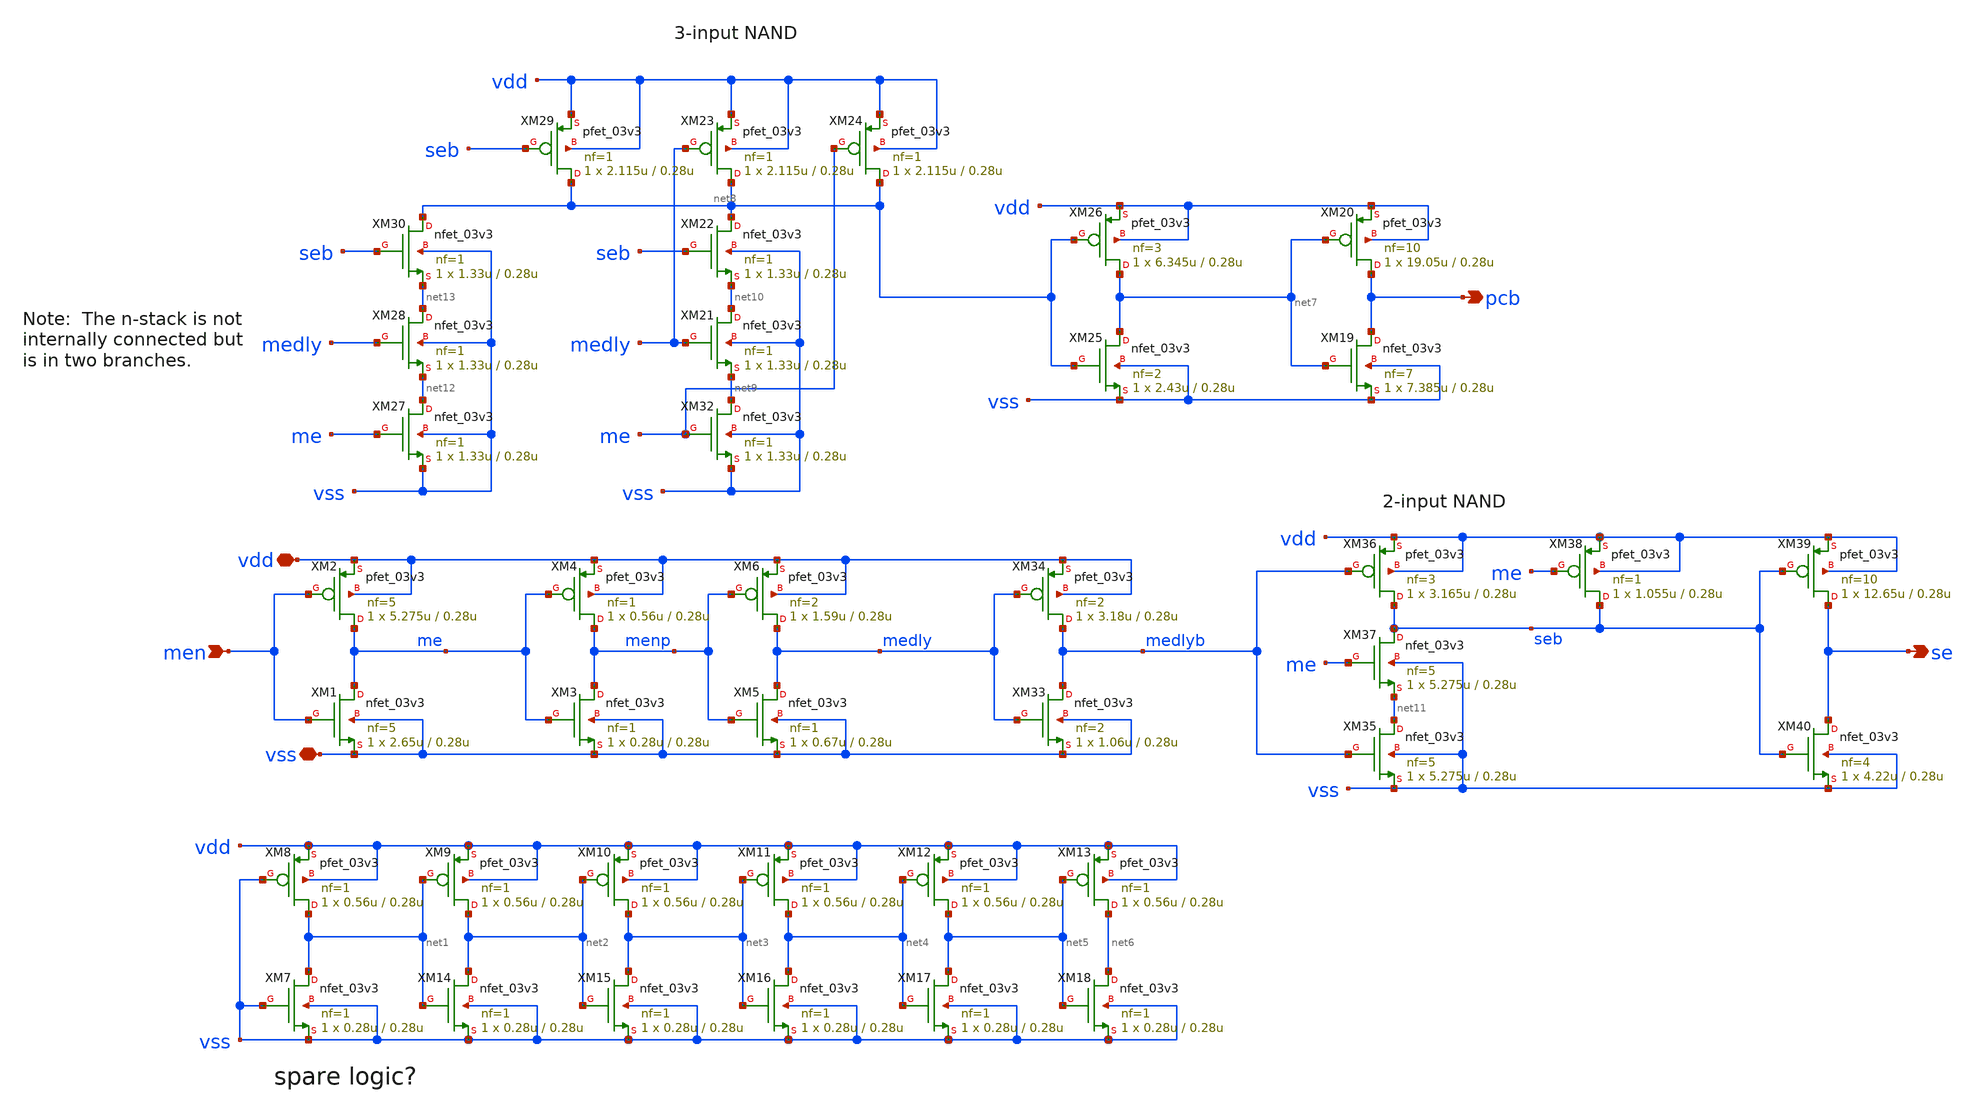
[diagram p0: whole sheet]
** sch_path: cells/gf180mcu_ocd_ip_sram__sram512x8m8wm1/xschem/sacntl_2_3v512x8m81.sch
**.subckt sacntl_2_3v512x8m81 men vdd vss se pcb
*.ipin men
*.iopin vdd
*.iopin vss
*.opin se
*.opin pcb
XM1 me men vss vss nfet_03v3 L=0.28u W=2.65u nf=5 ad='int((nf+1)/2) * W/nf * 0.18u' as='int((nf+2)/2) * W/nf * 0.18u'
+ pd='2*int((nf+1)/2) * (W/nf + 0.18u)' ps='2*int((nf+2)/2) * (W/nf + 0.18u)' nrd='0.18u / W' nrs='0.18u / W'
+ sa=0 sb=0 sd=0 m=1
XM2 me men vdd vdd pfet_03v3 L=0.28u W=5.275u nf=5 ad='int((nf+1)/2) * W/nf * 0.18u' as='int((nf+2)/2) * W/nf * 0.18u'
+ pd='2*int((nf+1)/2) * (W/nf + 0.18u)' ps='2*int((nf+2)/2) * (W/nf + 0.18u)' nrd='0.18u / W' nrs='0.18u / W'
+ sa=0 sb=0 sd=0 m=1
XM3 menp me vss vss nfet_03v3 L=0.28u W=0.28u nf=1 ad='int((nf+1)/2) * W/nf * 0.18u' as='int((nf+2)/2) * W/nf * 0.18u'
+ pd='2*int((nf+1)/2) * (W/nf + 0.18u)' ps='2*int((nf+2)/2) * (W/nf + 0.18u)' nrd='0.18u / W' nrs='0.18u / W'
+ sa=0 sb=0 sd=0 m=1
XM4 menp me vdd vdd pfet_03v3 L=0.28u W=0.56u nf=1 ad='int((nf+1)/2) * W/nf * 0.18u' as='int((nf+2)/2) * W/nf * 0.18u'
+ pd='2*int((nf+1)/2) * (W/nf + 0.18u)' ps='2*int((nf+2)/2) * (W/nf + 0.18u)' nrd='0.18u / W' nrs='0.18u / W'
+ sa=0 sb=0 sd=0 m=1
XM5 medly menp vss vss nfet_03v3 L=0.28u W=0.67u nf=1 ad='int((nf+1)/2) * W/nf * 0.18u' as='int((nf+2)/2) * W/nf * 0.18u'
+ pd='2*int((nf+1)/2) * (W/nf + 0.18u)' ps='2*int((nf+2)/2) * (W/nf + 0.18u)' nrd='0.18u / W' nrs='0.18u / W'
+ sa=0 sb=0 sd=0 m=1
XM6 medly menp vdd vdd pfet_03v3 L=0.28u W=1.59u nf=2 ad='int((nf+1)/2) * W/nf * 0.18u' as='int((nf+2)/2) * W/nf * 0.18u'
+ pd='2*int((nf+1)/2) * (W/nf + 0.18u)' ps='2*int((nf+2)/2) * (W/nf + 0.18u)' nrd='0.18u / W' nrs='0.18u / W'
+ sa=0 sb=0 sd=0 m=1
XM7 net1 vss vss vss nfet_03v3 L=0.28u W=0.28u nf=1 ad='int((nf+1)/2) * W/nf * 0.18u' as='int((nf+2)/2) * W/nf * 0.18u'
+ pd='2*int((nf+1)/2) * (W/nf + 0.18u)' ps='2*int((nf+2)/2) * (W/nf + 0.18u)' nrd='0.18u / W' nrs='0.18u / W'
+ sa=0 sb=0 sd=0 m=1
XM8 net1 vss vdd vdd pfet_03v3 L=0.28u W=0.56u nf=1 ad='int((nf+1)/2) * W/nf * 0.18u' as='int((nf+2)/2) * W/nf * 0.18u'
+ pd='2*int((nf+1)/2) * (W/nf + 0.18u)' ps='2*int((nf+2)/2) * (W/nf + 0.18u)' nrd='0.18u / W' nrs='0.18u / W'
+ sa=0 sb=0 sd=0 m=1
XM9 net2 net1 vdd vdd pfet_03v3 L=0.28u W=0.56u nf=1 ad='int((nf+1)/2) * W/nf * 0.18u' as='int((nf+2)/2) * W/nf * 0.18u'
+ pd='2*int((nf+1)/2) * (W/nf + 0.18u)' ps='2*int((nf+2)/2) * (W/nf + 0.18u)' nrd='0.18u / W' nrs='0.18u / W'
+ sa=0 sb=0 sd=0 m=1
XM10 net3 net2 vdd vdd pfet_03v3 L=0.28u W=0.56u nf=1 ad='int((nf+1)/2) * W/nf * 0.18u' as='int((nf+2)/2) * W/nf * 0.18u'
+ pd='2*int((nf+1)/2) * (W/nf + 0.18u)' ps='2*int((nf+2)/2) * (W/nf + 0.18u)' nrd='0.18u / W' nrs='0.18u / W'
+ sa=0 sb=0 sd=0 m=1
XM11 net4 net3 vdd vdd pfet_03v3 L=0.28u W=0.56u nf=1 ad='int((nf+1)/2) * W/nf * 0.18u' as='int((nf+2)/2) * W/nf * 0.18u'
+ pd='2*int((nf+1)/2) * (W/nf + 0.18u)' ps='2*int((nf+2)/2) * (W/nf + 0.18u)' nrd='0.18u / W' nrs='0.18u / W'
+ sa=0 sb=0 sd=0 m=1
XM12 net5 net4 vdd vdd pfet_03v3 L=0.28u W=0.56u nf=1 ad='int((nf+1)/2) * W/nf * 0.18u' as='int((nf+2)/2) * W/nf * 0.18u'
+ pd='2*int((nf+1)/2) * (W/nf + 0.18u)' ps='2*int((nf+2)/2) * (W/nf + 0.18u)' nrd='0.18u / W' nrs='0.18u / W'
+ sa=0 sb=0 sd=0 m=1
XM13 net6 net5 vdd vdd pfet_03v3 L=0.28u W=0.56u nf=1 ad='int((nf+1)/2) * W/nf * 0.18u' as='int((nf+2)/2) * W/nf * 0.18u'
+ pd='2*int((nf+1)/2) * (W/nf + 0.18u)' ps='2*int((nf+2)/2) * (W/nf + 0.18u)' nrd='0.18u / W' nrs='0.18u / W'
+ sa=0 sb=0 sd=0 m=1
XM14 net2 net1 vss vss nfet_03v3 L=0.28u W=0.28u nf=1 ad='int((nf+1)/2) * W/nf * 0.18u' as='int((nf+2)/2) * W/nf * 0.18u'
+ pd='2*int((nf+1)/2) * (W/nf + 0.18u)' ps='2*int((nf+2)/2) * (W/nf + 0.18u)' nrd='0.18u / W' nrs='0.18u / W'
+ sa=0 sb=0 sd=0 m=1
XM15 net3 net2 vss vss nfet_03v3 L=0.28u W=0.28u nf=1 ad='int((nf+1)/2) * W/nf * 0.18u' as='int((nf+2)/2) * W/nf * 0.18u'
+ pd='2*int((nf+1)/2) * (W/nf + 0.18u)' ps='2*int((nf+2)/2) * (W/nf + 0.18u)' nrd='0.18u / W' nrs='0.18u / W'
+ sa=0 sb=0 sd=0 m=1
XM16 net4 net3 vss vss nfet_03v3 L=0.28u W=0.28u nf=1 ad='int((nf+1)/2) * W/nf * 0.18u' as='int((nf+2)/2) * W/nf * 0.18u'
+ pd='2*int((nf+1)/2) * (W/nf + 0.18u)' ps='2*int((nf+2)/2) * (W/nf + 0.18u)' nrd='0.18u / W' nrs='0.18u / W'
+ sa=0 sb=0 sd=0 m=1
XM17 net5 net4 vss vss nfet_03v3 L=0.28u W=0.28u nf=1 ad='int((nf+1)/2) * W/nf * 0.18u' as='int((nf+2)/2) * W/nf * 0.18u'
+ pd='2*int((nf+1)/2) * (W/nf + 0.18u)' ps='2*int((nf+2)/2) * (W/nf + 0.18u)' nrd='0.18u / W' nrs='0.18u / W'
+ sa=0 sb=0 sd=0 m=1
XM18 net6 net5 vss vss nfet_03v3 L=0.28u W=0.28u nf=1 ad='int((nf+1)/2) * W/nf * 0.18u' as='int((nf+2)/2) * W/nf * 0.18u'
+ pd='2*int((nf+1)/2) * (W/nf + 0.18u)' ps='2*int((nf+2)/2) * (W/nf + 0.18u)' nrd='0.18u / W' nrs='0.18u / W'
+ sa=0 sb=0 sd=0 m=1
XM19 pcb net7 vss vss nfet_03v3 L=0.28u W=7.385u nf=7 ad='int((nf+1)/2) * W/nf * 0.18u' as='int((nf+2)/2) * W/nf * 0.18u'
+ pd='2*int((nf+1)/2) * (W/nf + 0.18u)' ps='2*int((nf+2)/2) * (W/nf + 0.18u)' nrd='0.18u / W' nrs='0.18u / W'
+ sa=0 sb=0 sd=0 m=1
XM20 pcb net7 vdd vdd pfet_03v3 L=0.28u W=19.05u nf=10 ad='int((nf+1)/2) * W/nf * 0.18u' as='int((nf+2)/2) * W/nf * 0.18u'
+ pd='2*int((nf+1)/2) * (W/nf + 0.18u)' ps='2*int((nf+2)/2) * (W/nf + 0.18u)' nrd='0.18u / W' nrs='0.18u / W'
+ sa=0 sb=0 sd=0 m=1
XM25 net7 net8 vss vss nfet_03v3 L=0.28u W=2.43u nf=2 ad='int((nf+1)/2) * W/nf * 0.18u' as='int((nf+2)/2) * W/nf * 0.18u'
+ pd='2*int((nf+1)/2) * (W/nf + 0.18u)' ps='2*int((nf+2)/2) * (W/nf + 0.18u)' nrd='0.18u / W' nrs='0.18u / W'
+ sa=0 sb=0 sd=0 m=1
XM26 net7 net8 vdd vdd pfet_03v3 L=0.28u W=6.345u nf=3 ad='int((nf+1)/2) * W/nf * 0.18u' as='int((nf+2)/2) * W/nf * 0.18u'
+ pd='2*int((nf+1)/2) * (W/nf + 0.18u)' ps='2*int((nf+2)/2) * (W/nf + 0.18u)' nrd='0.18u / W' nrs='0.18u / W'
+ sa=0 sb=0 sd=0 m=1
XM29 net8 seb vdd vdd pfet_03v3 L=0.28u W=2.115u nf=1 ad='int((nf+1)/2) * W/nf * 0.18u' as='int((nf+2)/2) * W/nf * 0.18u'
+ pd='2*int((nf+1)/2) * (W/nf + 0.18u)' ps='2*int((nf+2)/2) * (W/nf + 0.18u)' nrd='0.18u / W' nrs='0.18u / W'
+ sa=0 sb=0 sd=0 m=1
XM32 net9 me vss vss nfet_03v3 L=0.28u W=1.33u nf=1 ad='int((nf+1)/2) * W/nf * 0.18u' as='int((nf+2)/2) * W/nf * 0.18u'
+ pd='2*int((nf+1)/2) * (W/nf + 0.18u)' ps='2*int((nf+2)/2) * (W/nf + 0.18u)' nrd='0.18u / W' nrs='0.18u / W'
+ sa=0 sb=0 sd=0 m=1
XM33 medlyb medly vss vss nfet_03v3 L=0.28u W=1.06u nf=2 ad='int((nf+1)/2) * W/nf * 0.18u' as='int((nf+2)/2) * W/nf * 0.18u'
+ pd='2*int((nf+1)/2) * (W/nf + 0.18u)' ps='2*int((nf+2)/2) * (W/nf + 0.18u)' nrd='0.18u / W' nrs='0.18u / W'
+ sa=0 sb=0 sd=0 m=1
XM34 medlyb medly vdd vdd pfet_03v3 L=0.28u W=3.18u nf=2 ad='int((nf+1)/2) * W/nf * 0.18u' as='int((nf+2)/2) * W/nf * 0.18u'
+ pd='2*int((nf+1)/2) * (W/nf + 0.18u)' ps='2*int((nf+2)/2) * (W/nf + 0.18u)' nrd='0.18u / W' nrs='0.18u / W'
+ sa=0 sb=0 sd=0 m=1
XM35 net11 medlyb vss vss nfet_03v3 L=0.28u W=5.275u nf=5 ad='int((nf+1)/2) * W/nf * 0.18u' as='int((nf+2)/2) * W/nf * 0.18u'
+ pd='2*int((nf+1)/2) * (W/nf + 0.18u)' ps='2*int((nf+2)/2) * (W/nf + 0.18u)' nrd='0.18u / W' nrs='0.18u / W'
+ sa=0 sb=0 sd=0 m=1
XM36 seb medlyb vdd vdd pfet_03v3 L=0.28u W=3.165u nf=3 ad='int((nf+1)/2) * W/nf * 0.18u' as='int((nf+2)/2) * W/nf * 0.18u'
+ pd='2*int((nf+1)/2) * (W/nf + 0.18u)' ps='2*int((nf+2)/2) * (W/nf + 0.18u)' nrd='0.18u / W' nrs='0.18u / W'
+ sa=0 sb=0 sd=0 m=1
XM37 seb me net11 vss nfet_03v3 L=0.28u W=5.275u nf=5 ad='int((nf+1)/2) * W/nf * 0.18u' as='int((nf+2)/2) * W/nf * 0.18u'
+ pd='2*int((nf+1)/2) * (W/nf + 0.18u)' ps='2*int((nf+2)/2) * (W/nf + 0.18u)' nrd='0.18u / W' nrs='0.18u / W'
+ sa=0 sb=0 sd=0 m=1
XM38 seb me vdd vdd pfet_03v3 L=0.28u W=1.055u nf=1 ad='int((nf+1)/2) * W/nf * 0.18u' as='int((nf+2)/2) * W/nf * 0.18u'
+ pd='2*int((nf+1)/2) * (W/nf + 0.18u)' ps='2*int((nf+2)/2) * (W/nf + 0.18u)' nrd='0.18u / W' nrs='0.18u / W'
+ sa=0 sb=0 sd=0 m=1
XM39 se seb vdd vdd pfet_03v3 L=0.28u W=12.65u nf=10 ad='int((nf+1)/2) * W/nf * 0.18u' as='int((nf+2)/2) * W/nf * 0.18u'
+ pd='2*int((nf+1)/2) * (W/nf + 0.18u)' ps='2*int((nf+2)/2) * (W/nf + 0.18u)' nrd='0.18u / W' nrs='0.18u / W'
+ sa=0 sb=0 sd=0 m=1
XM40 se seb vss vss nfet_03v3 L=0.28u W=4.22u nf=4 ad='int((nf+1)/2) * W/nf * 0.18u' as='int((nf+2)/2) * W/nf * 0.18u'
+ pd='2*int((nf+1)/2) * (W/nf + 0.18u)' ps='2*int((nf+2)/2) * (W/nf + 0.18u)' nrd='0.18u / W' nrs='0.18u / W'
+ sa=0 sb=0 sd=0 m=1
XM21 net10 medly net9 vss nfet_03v3 L=0.28u W=1.33u nf=1 ad='int((nf+1)/2) * W/nf * 0.18u' as='int((nf+2)/2) * W/nf * 0.18u'
+ pd='2*int((nf+1)/2) * (W/nf + 0.18u)' ps='2*int((nf+2)/2) * (W/nf + 0.18u)' nrd='0.18u / W' nrs='0.18u / W'
+ sa=0 sb=0 sd=0 m=1
XM22 net8 seb net10 vss nfet_03v3 L=0.28u W=1.33u nf=1 ad='int((nf+1)/2) * W/nf * 0.18u' as='int((nf+2)/2) * W/nf * 0.18u'
+ pd='2*int((nf+1)/2) * (W/nf + 0.18u)' ps='2*int((nf+2)/2) * (W/nf + 0.18u)' nrd='0.18u / W' nrs='0.18u / W'
+ sa=0 sb=0 sd=0 m=1
XM23 net8 medly vdd vdd pfet_03v3 L=0.28u W=2.115u nf=1 ad='int((nf+1)/2) * W/nf * 0.18u' as='int((nf+2)/2) * W/nf * 0.18u'
+ pd='2*int((nf+1)/2) * (W/nf + 0.18u)' ps='2*int((nf+2)/2) * (W/nf + 0.18u)' nrd='0.18u / W' nrs='0.18u / W'
+ sa=0 sb=0 sd=0 m=1
XM24 net8 me vdd vdd pfet_03v3 L=0.28u W=2.115u nf=1 ad='int((nf+1)/2) * W/nf * 0.18u' as='int((nf+2)/2) * W/nf * 0.18u'
+ pd='2*int((nf+1)/2) * (W/nf + 0.18u)' ps='2*int((nf+2)/2) * (W/nf + 0.18u)' nrd='0.18u / W' nrs='0.18u / W'
+ sa=0 sb=0 sd=0 m=1
XM27 net12 me vss vss nfet_03v3 L=0.28u W=1.33u nf=1 ad='int((nf+1)/2) * W/nf * 0.18u' as='int((nf+2)/2) * W/nf * 0.18u'
+ pd='2*int((nf+1)/2) * (W/nf + 0.18u)' ps='2*int((nf+2)/2) * (W/nf + 0.18u)' nrd='0.18u / W' nrs='0.18u / W'
+ sa=0 sb=0 sd=0 m=1
XM28 net13 medly net12 vss nfet_03v3 L=0.28u W=1.33u nf=1 ad='int((nf+1)/2) * W/nf * 0.18u' as='int((nf+2)/2) * W/nf * 0.18u'
+ pd='2*int((nf+1)/2) * (W/nf + 0.18u)' ps='2*int((nf+2)/2) * (W/nf + 0.18u)' nrd='0.18u / W' nrs='0.18u / W'
+ sa=0 sb=0 sd=0 m=1
XM30 net8 seb net13 vss nfet_03v3 L=0.28u W=1.33u nf=1 ad='int((nf+1)/2) * W/nf * 0.18u' as='int((nf+2)/2) * W/nf * 0.18u'
+ pd='2*int((nf+1)/2) * (W/nf + 0.18u)' ps='2*int((nf+2)/2) * (W/nf + 0.18u)' nrd='0.18u / W' nrs='0.18u / W'
+ sa=0 sb=0 sd=0 m=1
**.ends
.end
